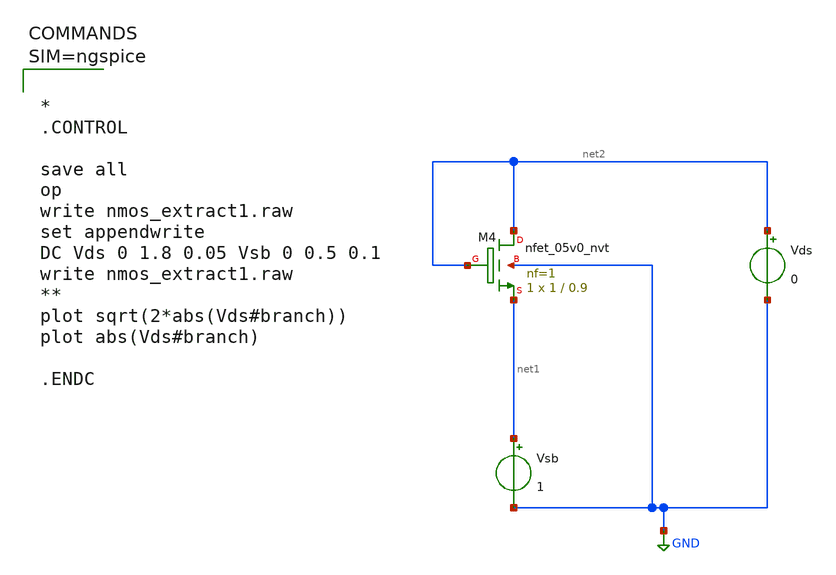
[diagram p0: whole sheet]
** sch_path: work/xschem/nmos_7.sch
**.subckt nmos_7
Vsb net1 GND 1
Vds net2 GND 0
XM4 net2 net2 net1 GND sky130_fd_pr__nfet_05v0_nvt L=0.9 W=1 nf=1 ad='int((1 + 1)/2) * 1 / 1 * 0.29'
+ as='int((1 + 2)/2) * 1 / 1 * 0.29' pd='2*int((1 + 1)/2) * (1 / 1 + 0.29)' ps='2*int((1 + 2)/2) * (1 / 1 + 0.29)'
+ nrd='0.29 / 1 ' nrs='0.29 / 1 ' sa=0 sb=0 sd=0 mult=1 m=1
**** begin user architecture code



*
.CONTROL

save all
op
write nmos_extract1.raw
set appendwrite
DC Vds 0 1.8 0.05 Vsb 0 0.5 0.1
write nmos_extract1.raw
**
plot sqrt(2*abs(Vds#branch))
plot abs(Vds#branch)

.ENDC




** opencircuitdesign pdks install
.lib $::SKYWATER_MODELS/sky130.lib.spice tt

**** end user architecture code
**.ends
.GLOBAL GND
.end
